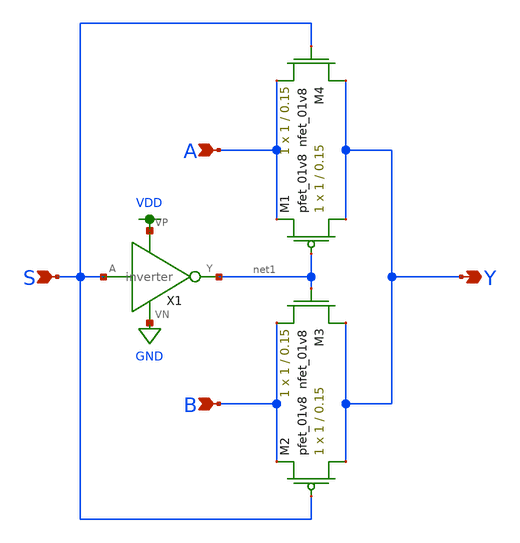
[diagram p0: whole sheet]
** sch_path: schematic/mux2.sch
**.subckt mux2 Y B A S
*.opin Y
*.ipin B
*.ipin A
*.ipin S
XM1 Y net1 A VDD sky130_fd_pr__pfet_01v8 L=0.15 W=1 nf=1 ad='int((nf+1)/2) * W/nf * 0.29' as='int((nf+2)/2) * W/nf * 0.29'
+ pd='2*int((nf+1)/2) * (W/nf + 0.29)' ps='2*int((nf+2)/2) * (W/nf + 0.29)' nrd='0.29 / W' nrs='0.29 / W'
+ sa=0 sb=0 sd=0 mult=1 m=1
XM2 Y S B VDD sky130_fd_pr__pfet_01v8 L=0.15 W=1 nf=1 ad='int((nf+1)/2) * W/nf * 0.29' as='int((nf+2)/2) * W/nf * 0.29'
+ pd='2*int((nf+1)/2) * (W/nf + 0.29)' ps='2*int((nf+2)/2) * (W/nf + 0.29)' nrd='0.29 / W' nrs='0.29 / W'
+ sa=0 sb=0 sd=0 mult=1 m=1
XM3 Y net1 B GND sky130_fd_pr__nfet_01v8 L=0.15 W=1 nf=1 ad='int((nf+1)/2) * W/nf * 0.29' as='int((nf+2)/2) * W/nf * 0.29'
+ pd='2*int((nf+1)/2) * (W/nf + 0.29)' ps='2*int((nf+2)/2) * (W/nf + 0.29)' nrd='0.29 / W' nrs='0.29 / W'
+ sa=0 sb=0 sd=0 mult=1 m=1
XM4 Y S A GND sky130_fd_pr__nfet_01v8 L=0.15 W=1 nf=1 ad='int((nf+1)/2) * W/nf * 0.29' as='int((nf+2)/2) * W/nf * 0.29'
+ pd='2*int((nf+1)/2) * (W/nf + 0.29)' ps='2*int((nf+2)/2) * (W/nf + 0.29)' nrd='0.29 / W' nrs='0.29 / W'
+ sa=0 sb=0 sd=0 mult=1 m=1
X1 S net1 VDD GND inverter
**.ends

* expanding   symbol:  /home/madvlsi/Documents/MADVLSI-Final_Project/schematic/inverter.sym # of
*+ pins=4
** sym_path: schematic/inverter.sym
** sch_path: schematic/inverter.sch
.subckt inverter A Y VP VN
*.opin Y
*.ipin A
*.iopin VP
*.iopin VN
XM3 Y A VP VDD sky130_fd_pr__pfet_01v8 L={Lp} W={Wp} nf=1 ad='int((nf+1)/2) * W/nf * 0.29' as='int((nf+2)/2) * W/nf * 0.29'
+ pd='2*int((nf+1)/2) * (W/nf + 0.29)' ps='2*int((nf+2)/2) * (W/nf + 0.29)' nrd='0.29 / W' nrs='0.29 / W'
+ sa=0 sb=0 sd=0 mult=1 m=1
XM4 Y A VP VDD sky130_fd_pr__pfet_01v8 L={Lp} W={Wp} nf=1 ad='int((nf+1)/2) * W/nf * 0.29' as='int((nf+2)/2) * W/nf * 0.29'
+ pd='2*int((nf+1)/2) * (W/nf + 0.29)' ps='2*int((nf+2)/2) * (W/nf + 0.29)' nrd='0.29 / W' nrs='0.29 / W'
+ sa=0 sb=0 sd=0 mult=1 m=1
XM5 Y A VN GND sky130_fd_pr__nfet_01v8 L={Lp} W={Wp} nf=1 ad='int((nf+1)/2) * W/nf * 0.29' as='int((nf+2)/2) * W/nf * 0.29'
+ pd='2*int((nf+1)/2) * (W/nf + 0.29)' ps='2*int((nf+2)/2) * (W/nf + 0.29)' nrd='0.29 / W' nrs='0.29 / W'
+ sa=0 sb=0 sd=0 mult=1 m=1
.ends

.GLOBAL VDD
.GLOBAL GND
.end
